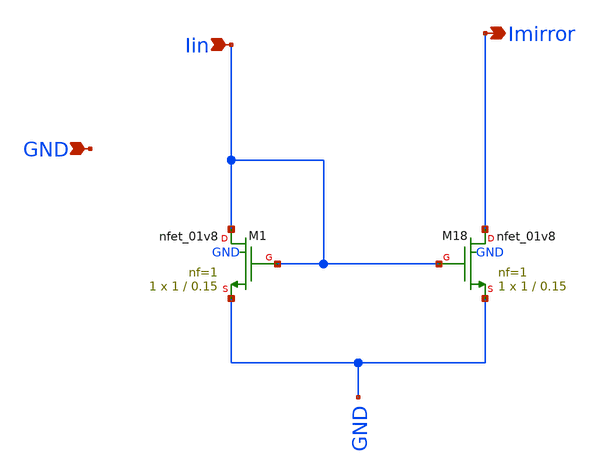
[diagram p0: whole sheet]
** sch_path: CurrentMirror.sch
**.subckt CurrentMirror Imirror GND Iin
*.opin Imirror
*.ipin GND
*.ipin Iin
XM18 Imirror Iin GND GND sky130_fd_pr__nfet_01v8 L=0.15 W=1 nf=1 ad='int((nf+1)/2) * W/nf * 0.29' as='int((nf+2)/2) * W/nf * 0.29'
+ pd='2*int((nf+1)/2) * (W/nf + 0.29)' ps='2*int((nf+2)/2) * (W/nf + 0.29)' nrd='0.29 / W' nrs='0.29 / W'
+ sa=0 sb=0 sd=0 mult=1 m=1
XM1 Iin Iin GND GND sky130_fd_pr__nfet_01v8 L=0.15 W=1 nf=1 ad='int((nf+1)/2) * W/nf * 0.29' as='int((nf+2)/2) * W/nf * 0.29'
+ pd='2*int((nf+1)/2) * (W/nf + 0.29)' ps='2*int((nf+2)/2) * (W/nf + 0.29)' nrd='0.29 / W' nrs='0.29 / W'
+ sa=0 sb=0 sd=0 mult=1 m=1
**.ends
.end
